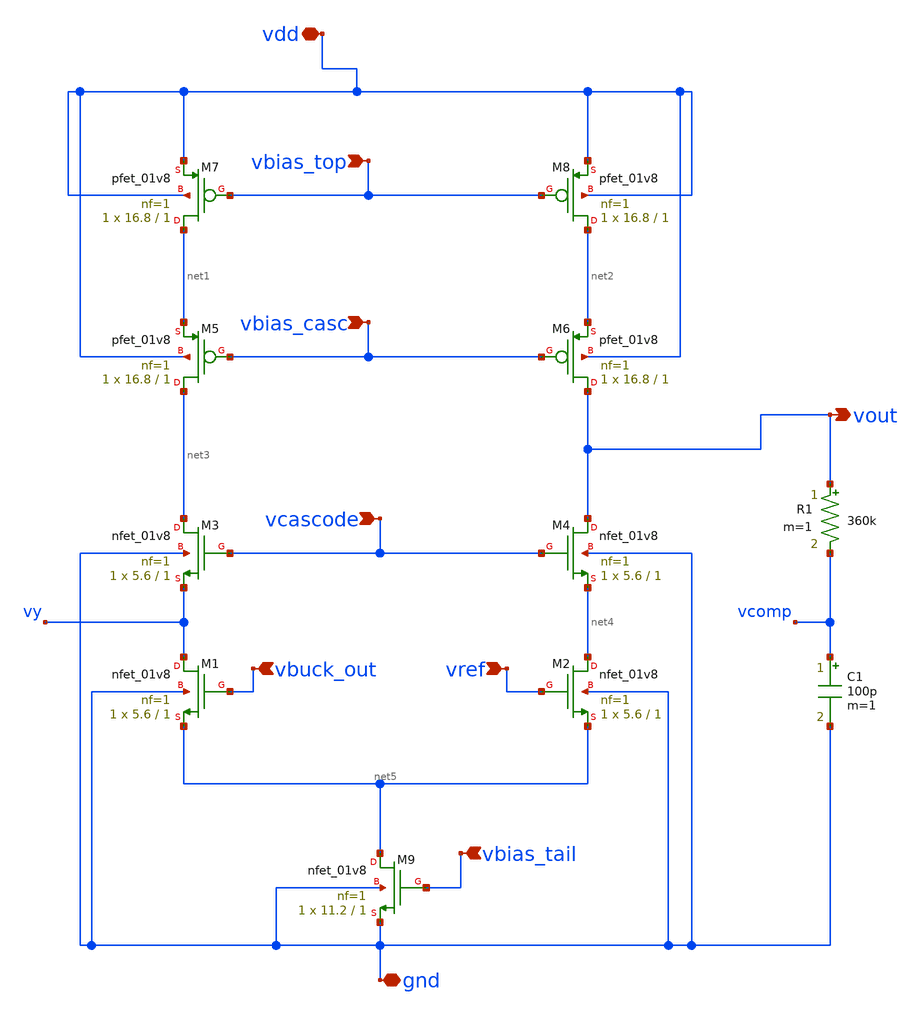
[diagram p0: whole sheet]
** sch_path: telescopic_ota.sch
**.subckt telescopic_ota vbias_top vbias_casc vcascode vbuck_out vref vbias_tail vout vdd gnd
*.ipin vbias_top
*.ipin vbias_casc
*.ipin vcascode
*.ipin vbuck_out
*.ipin vref
*.ipin vbias_tail
*.opin vout
*.iopin vdd
*.iopin gnd
XM3 net3 vcascode vy gnd sky130_fd_pr__nfet_01v8 L=1 W=5.6 nf=1 ad='int((1 + 1)/2) * 5.6 / 1 * 0.29'
+ as='int((1 + 2)/2) * 5.6 / 1 * 0.29' pd='2*int((1 + 1)/2) * (5.6 / 1 + 0.29)' ps='2*int((1 + 2)/2) * (5.6 / 1 + 0.29)'
+ nrd='0.29 / 5.6 ' nrs='0.29 / 5.6 ' sa=0 sb=0 sd=0 mult=1 m=1
XM8 net2 vbias_top vdd vdd sky130_fd_pr__pfet_01v8 L=1 W=16.8 nf=1 ad='int((1 + 1)/2) * 16.8 / 1 * 0.29'
+ as='int((1 + 2)/2) * 16.8 / 1 * 0.29' pd='2*int((1 + 1)/2) * (16.8 / 1 + 0.29)' ps='2*int((1 + 2)/2) * (16.8 / 1 + 0.29)'
+ nrd='0.29 / 16.8 ' nrs='0.29 / 16.8 ' sa=0 sb=0 sd=0 mult=1 m=1
XM7 net1 vbias_top vdd vdd sky130_fd_pr__pfet_01v8 L=1 W=16.8 nf=1 ad='int((1 + 1)/2) * 16.8 / 1 * 0.29'
+ as='int((1 + 2)/2) * 16.8 / 1 * 0.29' pd='2*int((1 + 1)/2) * (16.8 / 1 + 0.29)' ps='2*int((1 + 2)/2) * (16.8 / 1 + 0.29)'
+ nrd='0.29 / 16.8 ' nrs='0.29 / 16.8 ' sa=0 sb=0 sd=0 mult=1 m=1
XM5 net3 vbias_casc net1 vdd sky130_fd_pr__pfet_01v8 L=1 W=16.8 nf=1 ad='int((1 + 1)/2) * 16.8 / 1 * 0.29'
+ as='int((1 + 2)/2) * 16.8 / 1 * 0.29' pd='2*int((1 + 1)/2) * (16.8 / 1 + 0.29)' ps='2*int((1 + 2)/2) * (16.8 / 1 + 0.29)'
+ nrd='0.29 / 16.8 ' nrs='0.29 / 16.8 ' sa=0 sb=0 sd=0 mult=1 m=1
XM6 vout vbias_casc net2 vdd sky130_fd_pr__pfet_01v8 L=1 W=16.8 nf=1 ad='int((1 + 1)/2) * 16.8 / 1 * 0.29'
+ as='int((1 + 2)/2) * 16.8 / 1 * 0.29' pd='2*int((1 + 1)/2) * (16.8 / 1 + 0.29)' ps='2*int((1 + 2)/2) * (16.8 / 1 + 0.29)'
+ nrd='0.29 / 16.8 ' nrs='0.29 / 16.8 ' sa=0 sb=0 sd=0 mult=1 m=1
XM1 vy vbuck_out net5 gnd sky130_fd_pr__nfet_01v8 L=1 W=5.6 nf=1 ad='int((1 + 1)/2) * 5.6 / 1 * 0.29'
+ as='int((1 + 2)/2) * 5.6 / 1 * 0.29' pd='2*int((1 + 1)/2) * (5.6 / 1 + 0.29)' ps='2*int((1 + 2)/2) * (5.6 / 1 + 0.29)'
+ nrd='0.29 / 5.6 ' nrs='0.29 / 5.6 ' sa=0 sb=0 sd=0 mult=1 m=1
XM4 vout vcascode net4 gnd sky130_fd_pr__nfet_01v8 L=1 W=5.6 nf=1 ad='int((1 + 1)/2) * 5.6 / 1 * 0.29'
+ as='int((1 + 2)/2) * 5.6 / 1 * 0.29' pd='2*int((1 + 1)/2) * (5.6 / 1 + 0.29)' ps='2*int((1 + 2)/2) * (5.6 / 1 + 0.29)'
+ nrd='0.29 / 5.6 ' nrs='0.29 / 5.6 ' sa=0 sb=0 sd=0 mult=1 m=1
XM2 net4 vref net5 gnd sky130_fd_pr__nfet_01v8 L=1 W=5.6 nf=1 ad='int((1 + 1)/2) * 5.6 / 1 * 0.29' as='int((1 + 2)/2) * 5.6 / 1 * 0.29'
+ pd='2*int((1 + 1)/2) * (5.6 / 1 + 0.29)' ps='2*int((1 + 2)/2) * (5.6 / 1 + 0.29)' nrd='0.29 / 5.6 ' nrs='0.29 / 5.6 '
+ sa=0 sb=0 sd=0 mult=1 m=1
XM9 net5 vbias_tail gnd gnd sky130_fd_pr__nfet_01v8 L=1 W=11.2 nf=1 ad='int((1 + 1)/2) * 11.2 / 1 * 0.29'
+ as='int((1 + 2)/2) * 11.2 / 1 * 0.29' pd='2*int((1 + 1)/2) * (11.2 / 1 + 0.29)' ps='2*int((1 + 2)/2) * (11.2 / 1 + 0.29)'
+ nrd='0.29 / 11.2 ' nrs='0.29 / 11.2 ' sa=0 sb=0 sd=0 mult=1 m=1
R1 vout vcomp 360k m=1
C1 vcomp gnd 100p m=1
**.ends
.end
